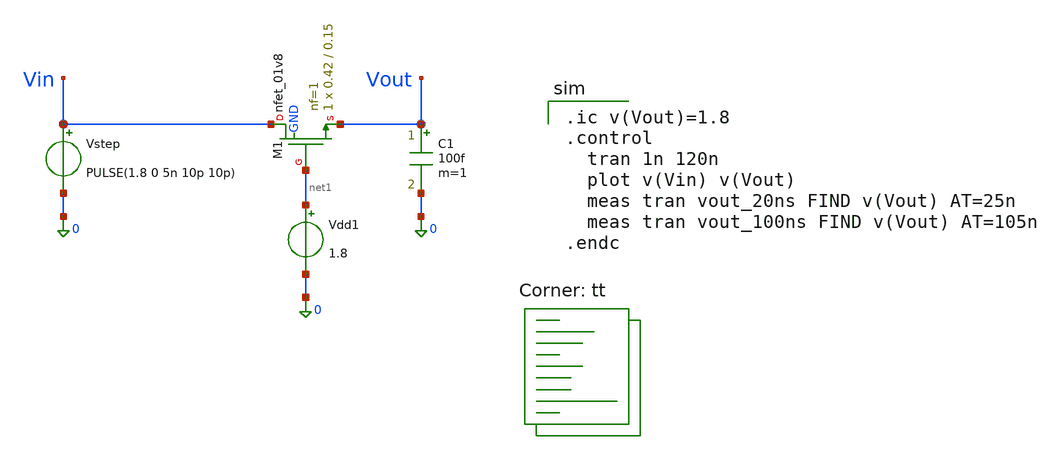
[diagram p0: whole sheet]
** sch_path: tutorial-1/source/q3c.sch
**.subckt q3c
XM1 Vin net1 Vout GND sky130_fd_pr__nfet_01v8 L=0.15 W=0.42 nf=1 ad='int((nf+1)/2) * W/nf * 0.29' as='int((nf+2)/2) * W/nf * 0.29'
+ pd='2*int((nf+1)/2) * (W/nf + 0.29)' ps='2*int((nf+2)/2) * (W/nf + 0.29)' nrd='0.29 / W' nrs='0.29 / W'
+ sa=0 sb=0 sd=0 mult=1 m=1
C1 Vout 0 100f m=1
Vstep Vin 0 PULSE(1.8 0 5n 10p 10p)
Vdd1 net1 0 1.8
**** begin user architecture code

.ic v(Vout)=1.8
.control
  tran 1n 120n
  plot v(Vin) v(Vout)
  meas tran vout_20ns FIND v(Vout) AT=25n
  meas tran vout_100ns FIND v(Vout) AT=105n
.endc

.lib $::SKYWATER_MODELS/sky130.lib.spice tt
**** end user architecture code
**.ends
.end
